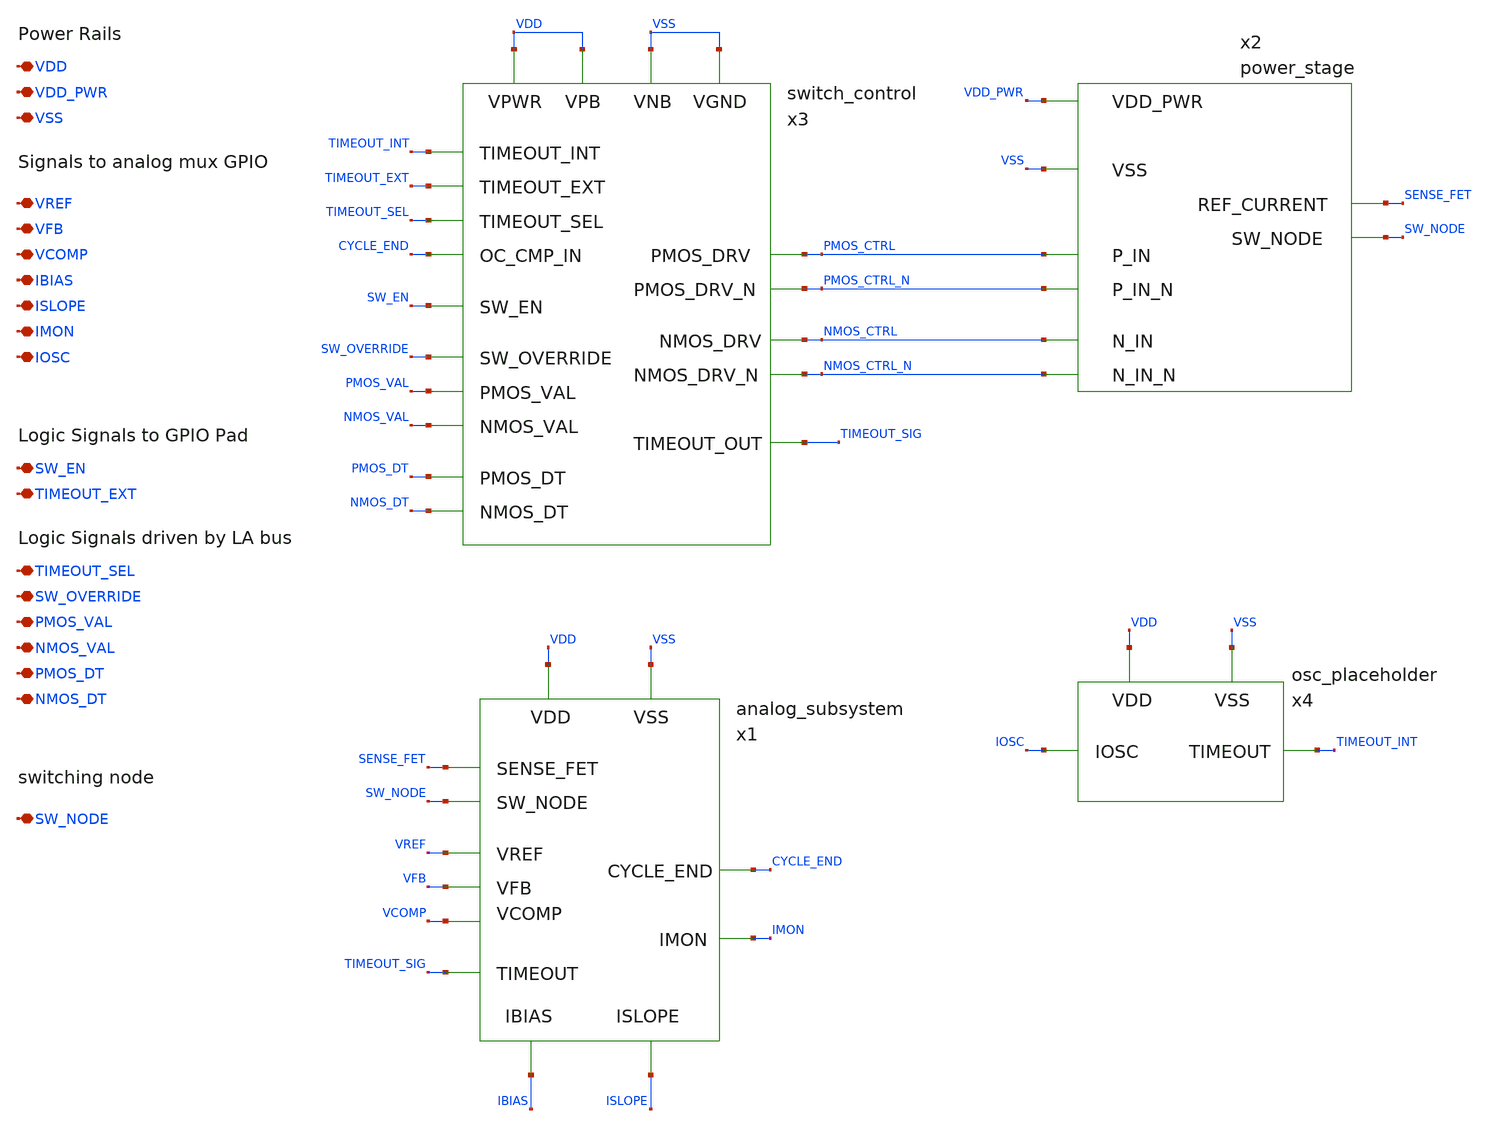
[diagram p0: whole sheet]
** sch_path: design/system/full_system.sch
**.subckt full_system VDD VSS IBIAS ISLOPE VREF VFB VCOMP VDD_PWR IMON SW_EN TIMEOUT_EXT TIMEOUT_SEL
*+ SW_OVERRIDE PMOS_VAL NMOS_VAL PMOS_DT NMOS_DT IOSC SW_NODE
*.iopin VDD
*.iopin VSS
*.iopin IBIAS
*.iopin ISLOPE
*.iopin VREF
*.iopin VFB
*.iopin VCOMP
*.iopin VDD_PWR
*.iopin IMON
*.iopin SW_EN
*.iopin TIMEOUT_EXT
*.iopin TIMEOUT_SEL
*.iopin SW_OVERRIDE
*.iopin PMOS_VAL
*.iopin NMOS_VAL
*.iopin PMOS_DT
*.iopin NMOS_DT
*.iopin IOSC
*.iopin SW_NODE
x1 VDD VSS IBIAS ISLOPE SENSE_FET SW_NODE VREF VFB VCOMP TIMEOUT_SIG CYCLE_END IMON analog_subsystem
x2 VDD_PWR VSS PMOS_CTRL PMOS_CTRL_N NMOS_CTRL SENSE_FET SW_NODE NMOS_CTRL_N power_stage
x3 VDD VDD VSS VSS TIMEOUT_INT CYCLE_END SW_EN SW_OVERRIDE PMOS_VAL NMOS_VAL PMOS_CTRL NMOS_CTRL
+ PMOS_DT NMOS_DT PMOS_CTRL_N NMOS_CTRL_N TIMEOUT_EXT TIMEOUT_SEL TIMEOUT_SIG switch_control
x4 VDD VSS IOSC TIMEOUT_INT osc_placeholder
**.ends
.end
